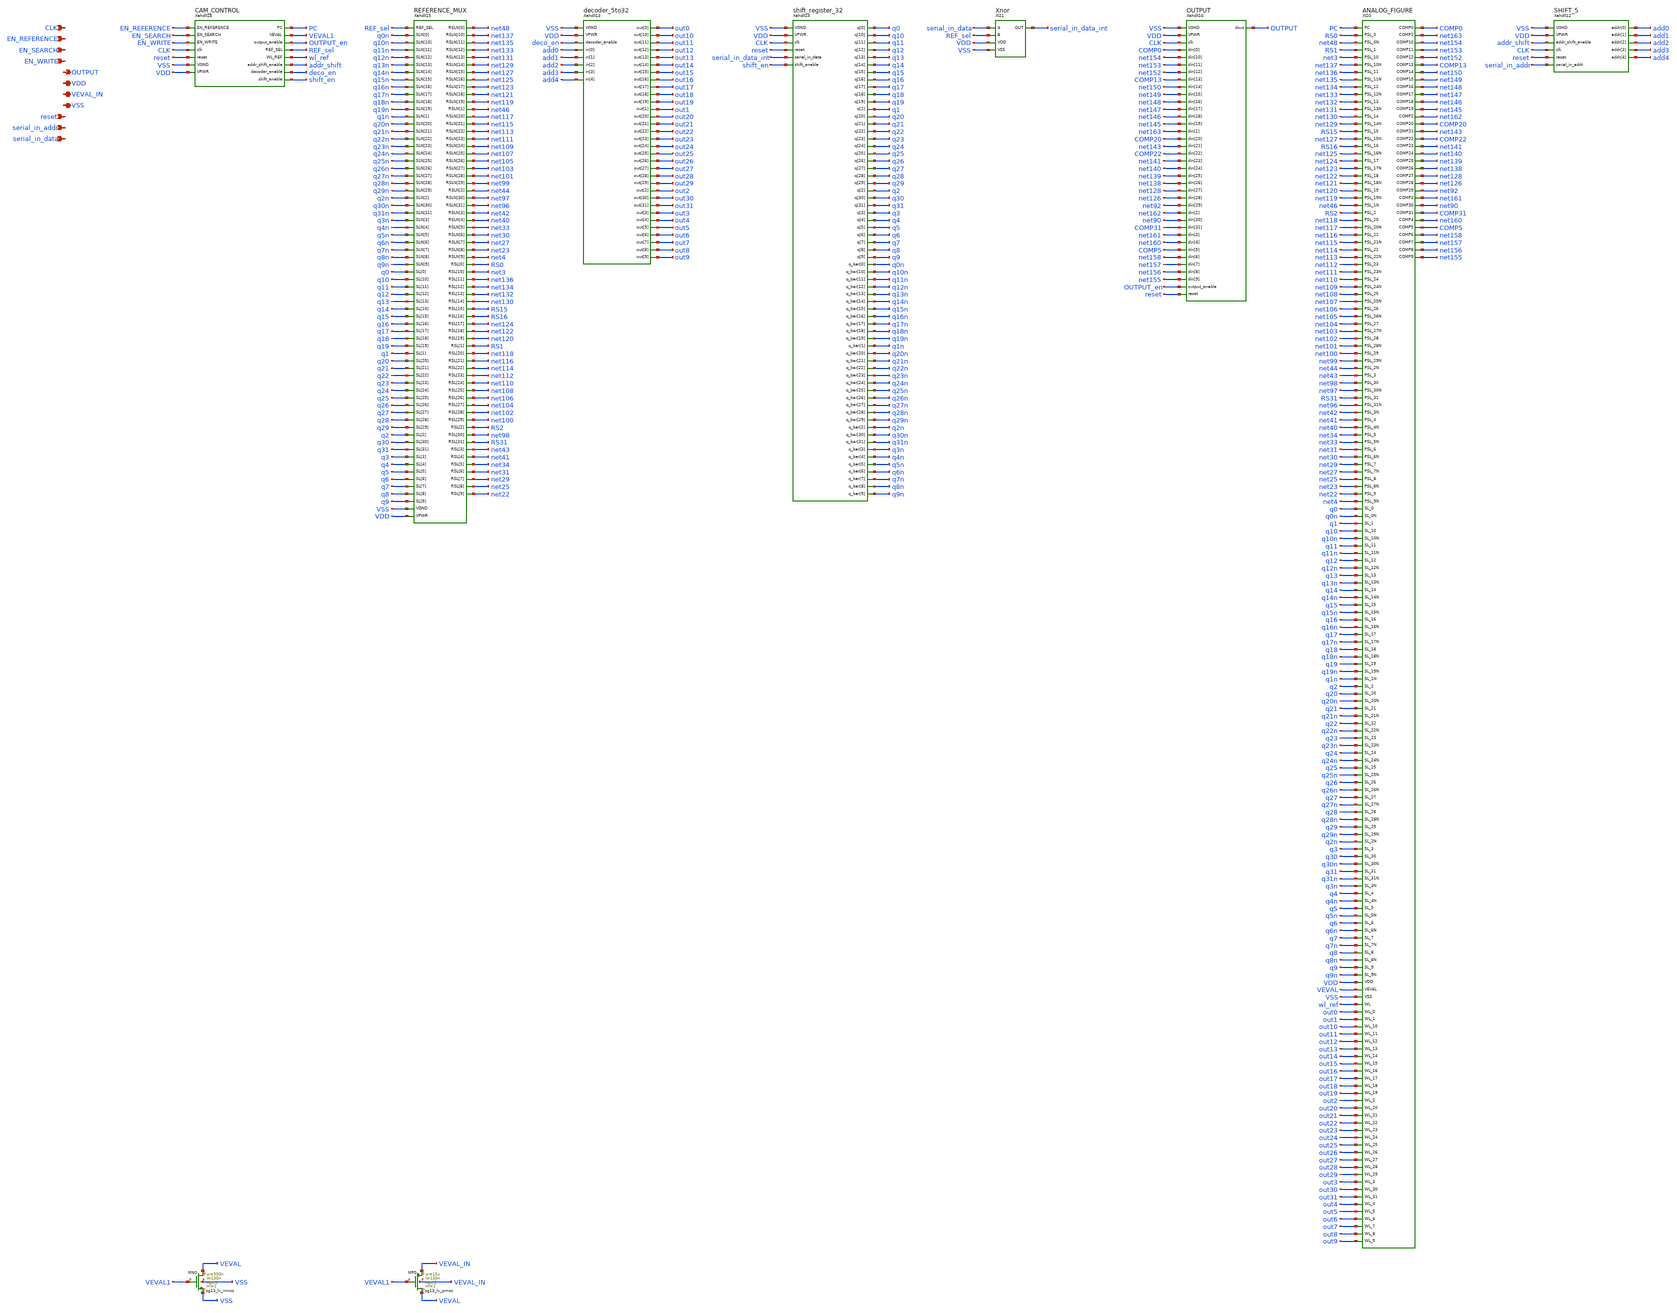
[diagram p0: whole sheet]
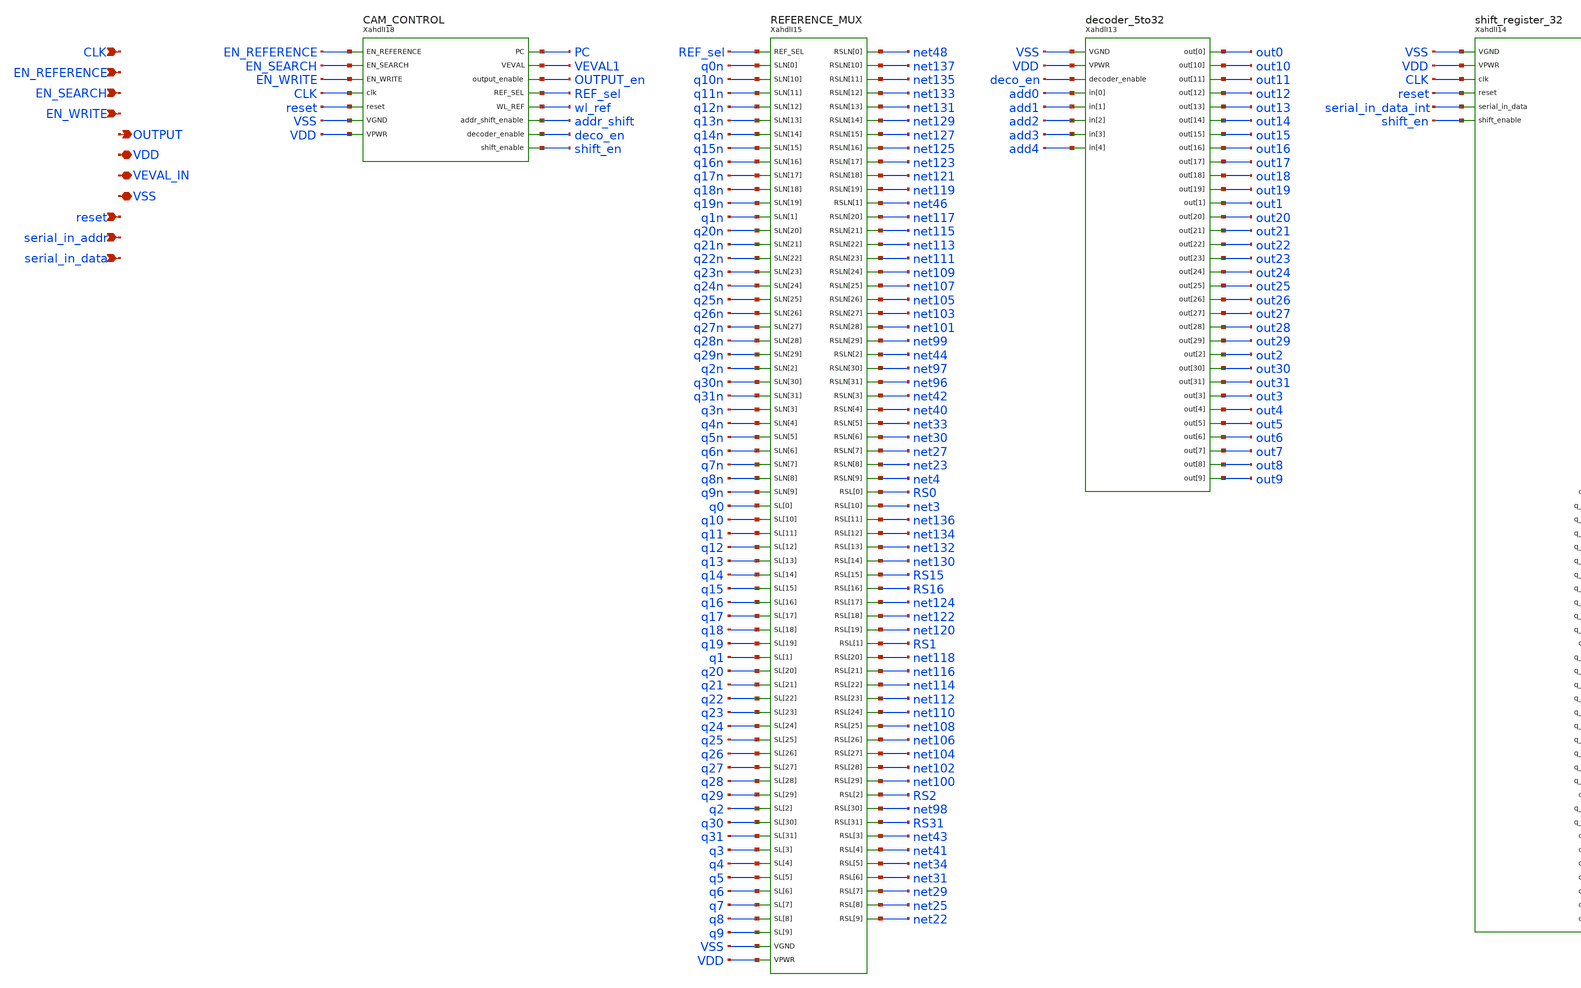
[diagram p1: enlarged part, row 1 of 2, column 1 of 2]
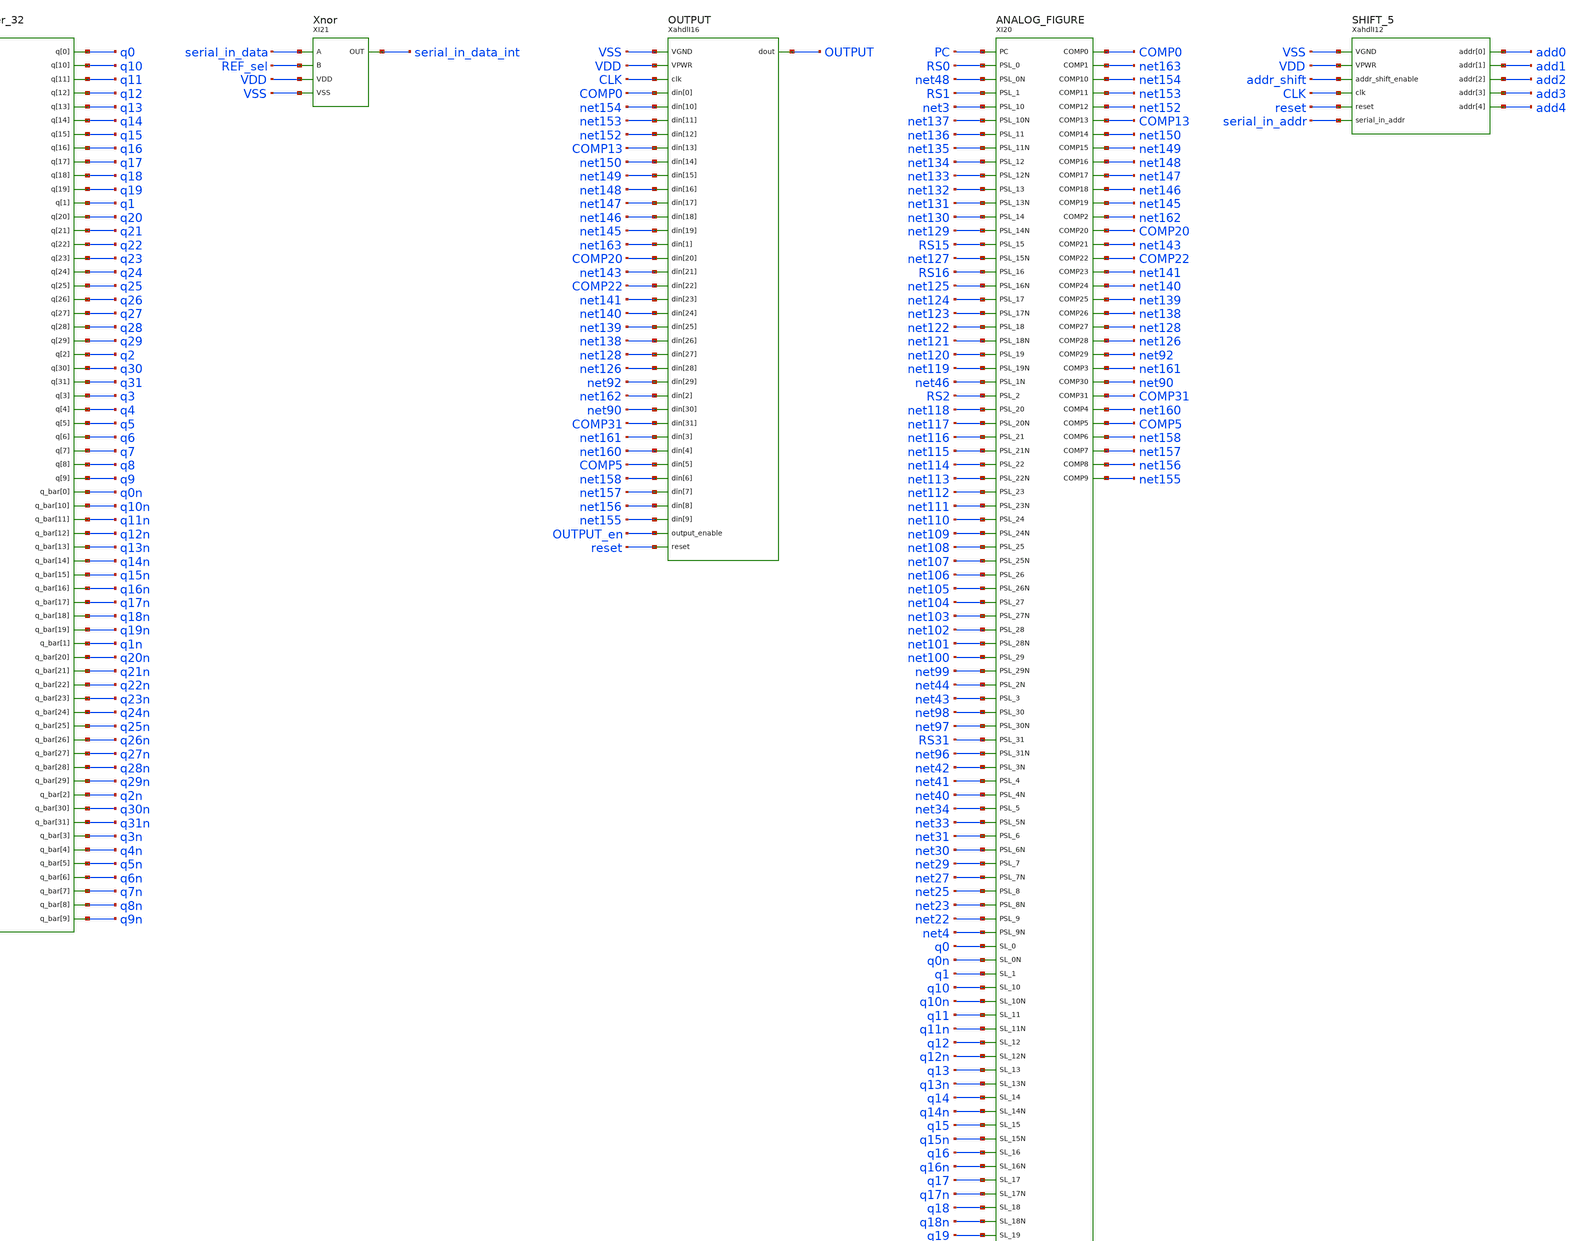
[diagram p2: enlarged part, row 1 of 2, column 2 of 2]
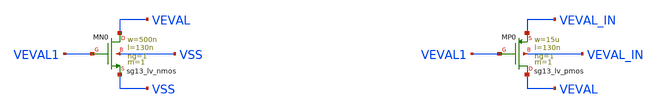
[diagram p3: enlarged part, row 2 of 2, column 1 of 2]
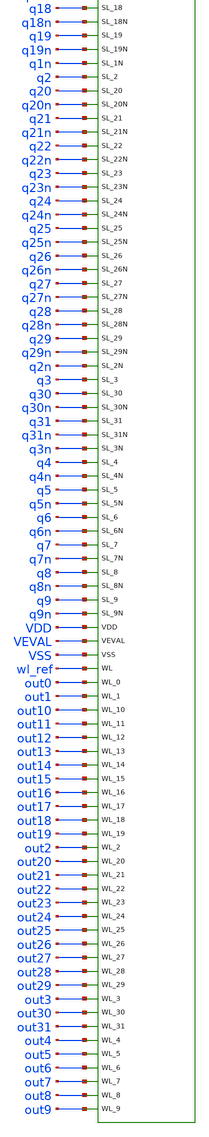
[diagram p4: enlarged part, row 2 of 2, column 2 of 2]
** sch_path: SoC6169-main/schematic/xschem/COMPLETE_PROYECT_FIG.sch
* Copyright 2026 USFQ CAM team
* Licensed under the Apache License, Version 2.0 (the "License");
* you may not use this file except in compliance with the License.
* You may obtain a copy of the License at
* https://www.apache.org/licenses/LICENSE-2.0
* Unless required by applicable law or agreed to in writing, software
* distributed under the License is distributed on an "AS IS" BASIS,
* WITHOUT WARRANTIES OR CONDITIONS OF ANY KIND, either express or implied.
* See the License for the specific language governing permissions and
* limitations under the License.
**.subckt COMPLETE_PROYECT_FIG CLK EN_REFERENCE EN_SEARCH EN_WRITE OUTPUT VDD VEVAL_IN VSS reset
*+ serial_in_addr serial_in_data
*.ipin CLK
*.ipin EN_REFERENCE
*.ipin EN_SEARCH
*.ipin EN_WRITE
*.opin OUTPUT
*.iopin VDD
*.iopin VEVAL_IN
*.iopin VSS
*.ipin reset
*.ipin serial_in_addr
*.ipin serial_in_data
XahdlI18 EN_REFERENCE EN_SEARCH EN_WRITE PC VEVAL1 CLK OUTPUT_en reset REF_sel wl_ref addr_shift
+ deco_en shift_en VSS VDD CAM_CONTROL
XahdlI15 REF_sel net48 net137 net135 net133 net131 net129 net127 net125 net123 net121 net119 net46
+ net117 net115 net113 net111 net109 net107 net105 net103 net101 net99 net44 net97 net96 net42 net40 net33
+ net30 net27 net23 net4 RS0 net3 net136 net134 net132 net130 RS15 RS16 net124 net122 net120 RS1 net118
+ net116 net114 net112 net110 net108 net106 net104 net102 net100 RS2 net98 RS31 net43 net41 net34 net31
+ net29 net25 net22 q0n q10n q11n q12n q13n q14n q15n q16n q17n q18n q19n q1n q20n q21n q22n q23n q24n q25n
+ q26n q27n q28n q29n q2n q30n q31n q3n q4n q5n q6n q7n q8n q9n q0 q10 q11 q12 q13 q14 q15 q16 q17 q18 q19
+ q1 q20 q21 q22 q23 q24 q25 q26 q27 q28 q29 q2 q30 q31 q3 q4 q5 q6 q7 q8 q9 VSS VDD REFERENCE_MUX
XahdlI13 VSS VDD deco_en add0 add1 add2 add3 add4 out0 out10 out11 out12 out13 out14 out15 out16
+ out17 out18 out19 out1 out20 out21 out22 out23 out24 out25 out26 out27 out28 out29 out2 out30 out31 out3
+ out4 out5 out6 out7 out8 out9 decoder_5to32
XahdlI14 VSS VDD CLK q0 q10 q11 q12 q13 q14 q15 q16 q17 q18 q19 q1 q20 q21 q22 q23 q24 q25 q26 q27
+ q28 q29 q2 q30 q31 q3 q4 q5 q6 q7 q8 q9 q0n q10n q11n q12n q13n q14n q15n q16n q17n q18n q19n q1n q20n
+ q21n q22n q23n q24n q25n q26n q27n q28n q29n q2n q30n q31n q3n q4n q5n q6n q7n q8n q9n reset
+ serial_in_data_int shift_en shift_register_32
XI21 serial_in_data REF_sel serial_in_data_int VDD VSS Xnor
XahdlI16 VSS VDD CLK COMP0 net154 net153 net152 COMP13 net150 net149 net148 net147 net146 net145
+ net163 COMP20 net143 COMP22 net141 net140 net139 net138 net128 net126 net92 net162 net90 COMP31 net161
+ net160 COMP5 net158 net157 net156 net155 OUTPUT OUTPUT_en reset OUTPUT
XI20 COMP0 net163 net154 net153 net152 COMP13 net150 net149 net148 net147 net146 net145 net162
+ COMP20 net143 COMP22 net141 net140 net139 net138 net128 net126 net92 net161 net90 COMP31 net160 COMP5
+ net158 net157 net156 net155 PC RS0 net48 RS1 net3 net137 net136 net135 net134 net133 net132 net131 net130
+ net129 RS15 net127 RS16 net125 net124 net123 net122 net121 net120 net119 net46 RS2 net118 net117 net116
+ net115 net114 net113 net112 net111 net110 net109 net108 net107 net106 net105 net104 net103 net102 net101
+ net100 net99 net44 net43 net98 net97 RS31 net96 net42 net41 net40 net34 net33 net31 net30 net29 net27
+ net25 net23 net22 net4 q0 q0n q1 q10 q10n q11 q11n q12 q12n q13 q13n q14 q14n q15 q15n q16 q16n q17 q17n
+ q18 q18n q19 q19n q1n q2 q20 q20n q21 q21n q22 q22n q23 q23n q24 q24n q25 q25n q26 q26n q27 q27n q28
+ q28n q29 q29n q2n q3 q30 q30n q31 q31n q3n q4 q4n q5 q5n q6 q6n q7 q7n q8 q8n q9 q9n VDD VEVAL VSS
+ wl_ref out0 out1 out10 out11 out12 out13 out14 out15 out16 out17 out18 out19 out2 out20 out21 out22 out23
+ out24 out25 out26 out27 out28 out29 out3 out30 out31 out4 out5 out6 out7 out8 out9 ANALOG_FIGURE
XahdlI12 VSS VDD add0 add1 add2 add3 add4 addr_shift CLK reset serial_in_addr SHIFT_5
XMN0 VEVAL VEVAL1 VSS VSS sg13_lv_nmos w=500n l=130n ng=1 m=1 mm_ok=1
XMP0 VEVAL VEVAL1 VEVAL_IN VEVAL_IN sg13_lv_pmos w=15u l=130n ng=1 m=1 mm_ok=1
**.ends
.end
